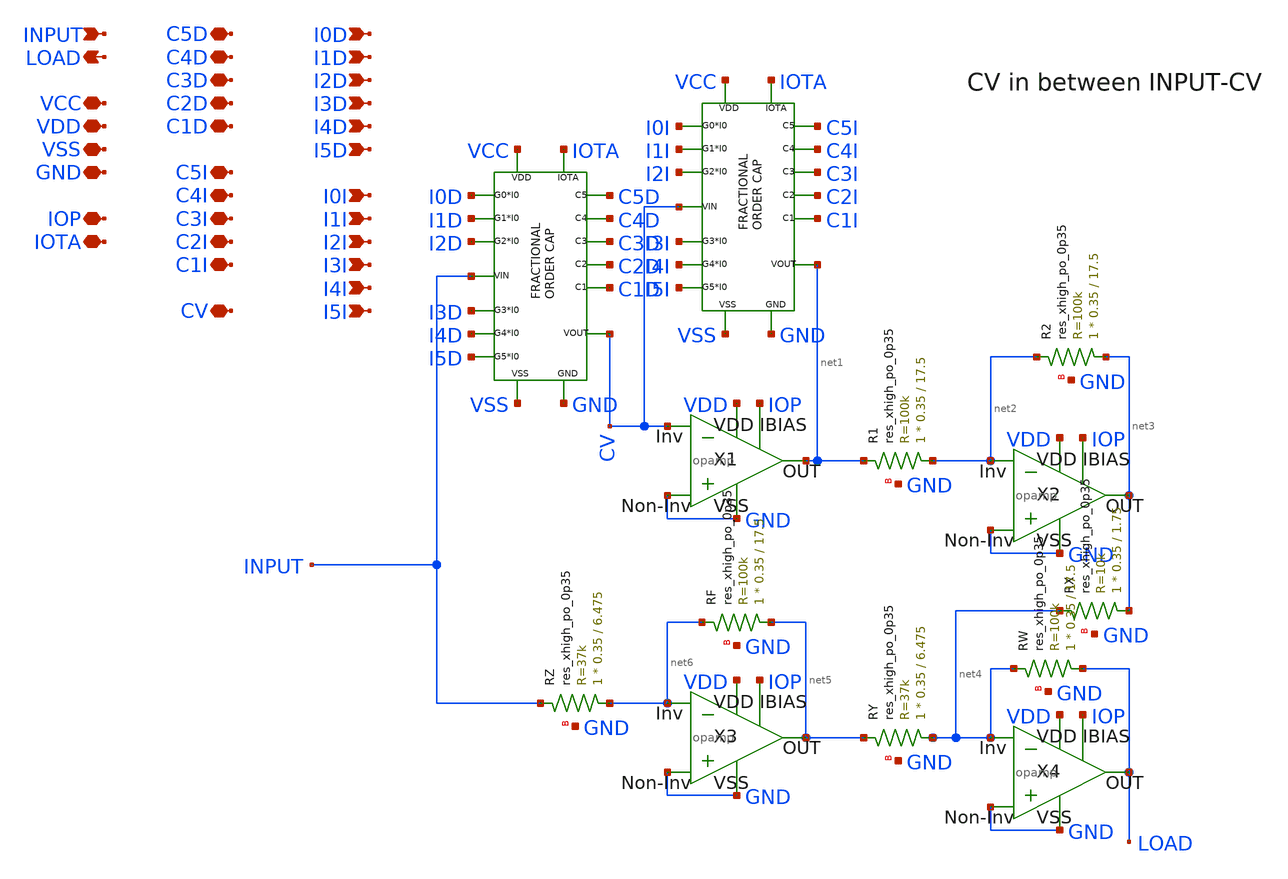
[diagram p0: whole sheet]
** sch_path: Fractional Order PID/FOPID/FOPID.sch
**.subckt FOPID VCC VDD VSS GND IOP IOTA INPUT LOAD C5D C4D C3D C2D C1D C5I C4I C3I C2I C1I I0D I1D
*+ I2D I3D I4D I5D I0I I1I I2I I3I I4I I5I CV
*.iopin VCC
*.iopin VDD
*.iopin VSS
*.iopin GND
*.iopin IOP
*.iopin IOTA
*.ipin INPUT
*.opin LOAD
*.iopin C5D
*.iopin C4D
*.iopin C3D
*.iopin C2D
*.iopin C1D
*.iopin C5I
*.iopin C4I
*.iopin C3I
*.iopin C2I
*.iopin C1I
*.ipin I0D
*.ipin I1D
*.ipin I2D
*.ipin I3D
*.ipin I4D
*.ipin I5D
*.ipin I0I
*.ipin I1I
*.ipin I2I
*.ipin I3I
*.ipin I4I
*.ipin I5I
*.iopin CV
X1 CV GND GND VDD net1 IOP opamp
X2 net2 GND GND VDD net3 IOP opamp
X3 net6 GND GND VDD net5 IOP opamp
X4 net4 GND GND VDD LOAD IOP opamp
X5 VCC IOTA CV GND VSS I5D I4D I3D I2D I1D I0D INPUT C5D C4D C3D C2D C1D Fractional_diff
X6 VCC IOTA net1 GND VSS I5I I4I I3I I2I I1I I0I CV C5I C4I C3I C2I C1I Fractional_diff
XR1 net2 net1 GND sky130_fd_pr__res_xhigh_po_0p35 L=17.5 mult=1 m=1
XR2 net3 net2 GND sky130_fd_pr__res_xhigh_po_0p35 L=17.5 mult=1 m=1
XRX net3 net4 GND sky130_fd_pr__res_xhigh_po_0p35 L=1.75 mult=1 m=1
XRW LOAD net4 GND sky130_fd_pr__res_xhigh_po_0p35 L=17.5 mult=1 m=1
XRY net4 net5 GND sky130_fd_pr__res_xhigh_po_0p35 L=6.475 mult=1 m=1
XRF net5 net6 GND sky130_fd_pr__res_xhigh_po_0p35 L=17.5 mult=1 m=1
XRZ net6 INPUT GND sky130_fd_pr__res_xhigh_po_0p35 L=6.475 mult=1 m=1
**.ends

* expanding   symbol:  /home/parallels/OPAMP/opamp.sym # of pins=6
** sym_path: /home/parallels/OPAMP/opamp.sym
** sch_path: /home/parallels/OPAMP/opamp.sch
.subckt opamp VN VP GND VDD VOUT IBIAS
*.iopin VDD
*.iopin IBIAS
*.ipin VN
*.ipin VP
*.iopin GND
*.opin VOUT
XM1 IBIAS IBIAS VDD VDD sky130_fd_pr__pfet_01v8 L=0.3 W=3 nf=1 ad='int((nf+1)/2) * W/nf * 0.29' as='int((nf+2)/2) * W/nf * 0.29'
+ pd='2*int((nf+1)/2) * (W/nf + 0.29)' ps='2*int((nf+2)/2) * (W/nf + 0.29)' nrd='0.29 / W' nrs='0.29 / W'
+ sa=0 sb=0 sd=0 mult=1 m=1
XM2 net1 IBIAS VDD VDD sky130_fd_pr__pfet_01v8 L=0.3 W=30 nf=5 ad='int((nf+1)/2) * W/nf * 0.29' as='int((nf+2)/2) * W/nf * 0.29'
+ pd='2*int((nf+1)/2) * (W/nf + 0.29)' ps='2*int((nf+2)/2) * (W/nf + 0.29)' nrd='0.29 / W' nrs='0.29 / W'
+ sa=0 sb=0 sd=0 mult=1 m=1
XM3 net2 VN net1 VDD sky130_fd_pr__pfet_01v8 L=0.3 W=36 nf=6 ad='int((nf+1)/2) * W/nf * 0.29' as='int((nf+2)/2) * W/nf * 0.29'
+ pd='2*int((nf+1)/2) * (W/nf + 0.29)' ps='2*int((nf+2)/2) * (W/nf + 0.29)' nrd='0.29 / W' nrs='0.29 / W'
+ sa=0 sb=0 sd=0 mult=1 m=1
XM4 o1 VP net1 VDD sky130_fd_pr__pfet_01v8 L=0.3 W=36 nf=6 ad='int((nf+1)/2) * W/nf * 0.29' as='int((nf+2)/2) * W/nf * 0.29'
+ pd='2*int((nf+1)/2) * (W/nf + 0.29)' ps='2*int((nf+2)/2) * (W/nf + 0.29)' nrd='0.29 / W' nrs='0.29 / W'
+ sa=0 sb=0 sd=0 mult=1 m=1
XM5 net2 net2 GND GND sky130_fd_pr__nfet_01v8 L=0.3 W=6 nf=2 ad='int((nf+1)/2) * W/nf * 0.29' as='int((nf+2)/2) * W/nf * 0.29'
+ pd='2*int((nf+1)/2) * (W/nf + 0.29)' ps='2*int((nf+2)/2) * (W/nf + 0.29)' nrd='0.29 / W' nrs='0.29 / W'
+ sa=0 sb=0 sd=0 mult=1 m=1
XM6 o1 net2 GND GND sky130_fd_pr__nfet_01v8 L=0.3 W=6 nf=2 ad='int((nf+1)/2) * W/nf * 0.29' as='int((nf+2)/2) * W/nf * 0.29'
+ pd='2*int((nf+1)/2) * (W/nf + 0.29)' ps='2*int((nf+2)/2) * (W/nf + 0.29)' nrd='0.29 / W' nrs='0.29 / W'
+ sa=0 sb=0 sd=0 mult=1 m=1
XM7 VOUT IBIAS VDD VDD sky130_fd_pr__pfet_01v8 L=0.3 W=45 nf=9 ad='int((nf+1)/2) * W/nf * 0.29' as='int((nf+2)/2) * W/nf * 0.29'
+ pd='2*int((nf+1)/2) * (W/nf + 0.29)' ps='2*int((nf+2)/2) * (W/nf + 0.29)' nrd='0.29 / W' nrs='0.29 / W'
+ sa=0 sb=0 sd=0 mult=1 m=1
XM8 VOUT o1 GND GND sky130_fd_pr__nfet_01v8 L=0.3 W=18 nf=3 ad='int((nf+1)/2) * W/nf * 0.29' as='int((nf+2)/2) * W/nf * 0.29'
+ pd='2*int((nf+1)/2) * (W/nf + 0.29)' ps='2*int((nf+2)/2) * (W/nf + 0.29)' nrd='0.29 / W' nrs='0.29 / W'
+ sa=0 sb=0 sd=0 mult=1 m=1
XC2 o1 VOUT sky130_fd_pr__cap_mim_m3_1 W=11 L=22 MF=1 m=1
.ends


* expanding   symbol:  /home/parallels/Fractional Differentiator/Fractional_diff.sym # of pins=17
** sym_path: Fractional Order PID/Fractional Order Capacitor/Fractional_diff.sym
** sch_path: Fractional Order PID/Fractional Order Capacitor/Fractional_diff.sch
.subckt Fractional_diff VDD IOTA VOUT GND VSS I5 I4 I3 I2 I1 I0 VIN C5 C4 C3 C2 C1
*.ipin VIN
*.ipin I0
*.ipin I1
*.ipin I2
*.ipin I3
*.ipin I4
*.ipin I5
*.iopin IOTA
*.iopin VDD
*.iopin VSS
*.iopin GND
*.opin VOUT
*.iopin C5
*.iopin C4
*.iopin C3
*.iopin C2
*.iopin C1
X1 IOTA VDD C5 VSS VOUT GND ota3
X2 IOTA VDD C4 VSS VOUT C5 ota3
X3 IOTA VDD C3 VSS VOUT C4 ota3
X4 IOTA VDD C2 VSS VOUT C3 ota3
X5 IOTA VDD C1 VSS VOUT C2 ota3
X6 IOTA VDD VOUT VSS GND C1 ota3
X7 IOTA VDD VOUT VSS VOUT GND ota3
X8 I5 VDD VOUT VSS GND VIN ota3
X9 I4 VDD C1 VSS GND VIN ota3
X10 I3 VDD C2 VSS GND VIN ota3
X11 I2 VDD C3 VSS GND VIN ota3
X12 I1 VDD C4 VSS GND VIN ota3
X13 I0 VDD C5 VSS GND VIN ota3
.ends


* expanding   symbol:  /home/parallels/OTA/ota3.sym # of pins=6
** sym_path: Fractional Order PID/OTA/ota3.sym
** sch_path: Fractional Order PID/OTA/ota3.sch
.subckt ota3 IBIAS VDD IOUT VSS VN VP
*.iopin VP
*.iopin IBIAS
*.iopin IOUT
*.iopin VDD
*.iopin VSS
*.iopin VN
XMp1 net1 net1 VDD VDD sky130_fd_pr__pfet_01v8 L=2 W=10 nf=2 ad='int((nf+1)/2) * W/nf * 0.29' as='int((nf+2)/2) * W/nf * 0.29'
+ pd='2*int((nf+1)/2) * (W/nf + 0.29)' ps='2*int((nf+2)/2) * (W/nf + 0.29)' nrd='0.29 / W' nrs='0.29 / W'
+ sa=0 sb=0 sd=0 mult=1 m=1
XMp2 IOUT net1 VDD VDD sky130_fd_pr__pfet_01v8 L=2 W=10 nf=2 ad='int((nf+1)/2) * W/nf * 0.29' as='int((nf+2)/2) * W/nf * 0.29'
+ pd='2*int((nf+1)/2) * (W/nf + 0.29)' ps='2*int((nf+2)/2) * (W/nf + 0.29)' nrd='0.29 / W' nrs='0.29 / W'
+ sa=0 sb=0 sd=0 mult=1 m=1
XMn1 net1 VP net2 net2 sky130_fd_pr__nfet_01v8 L=5 W=25 nf=5 ad='int((nf+1)/2) * W/nf * 0.29' as='int((nf+2)/2) * W/nf * 0.29'
+ pd='2*int((nf+1)/2) * (W/nf + 0.29)' ps='2*int((nf+2)/2) * (W/nf + 0.29)' nrd='0.29 / W' nrs='0.29 / W'
+ sa=0 sb=0 sd=0 mult=1 m=1
XMn2 IOUT VN net2 net2 sky130_fd_pr__nfet_01v8 L=5 W=5 nf=1 ad='int((nf+1)/2) * W/nf * 0.29' as='int((nf+2)/2) * W/nf * 0.29'
+ pd='2*int((nf+1)/2) * (W/nf + 0.29)' ps='2*int((nf+2)/2) * (W/nf + 0.29)' nrd='0.29 / W' nrs='0.29 / W'
+ sa=0 sb=0 sd=0 mult=1 m=1
XMn3 net1 VP net3 net3 sky130_fd_pr__nfet_01v8 L=5 W=5 nf=1 ad='int((nf+1)/2) * W/nf * 0.29' as='int((nf+2)/2) * W/nf * 0.29'
+ pd='2*int((nf+1)/2) * (W/nf + 0.29)' ps='2*int((nf+2)/2) * (W/nf + 0.29)' nrd='0.29 / W' nrs='0.29 / W'
+ sa=0 sb=0 sd=0 mult=1 m=1
XMn4 IOUT VN net3 net3 sky130_fd_pr__nfet_01v8 L=5 W=25 nf=5 ad='int((nf+1)/2) * W/nf * 0.29' as='int((nf+2)/2) * W/nf * 0.29'
+ pd='2*int((nf+1)/2) * (W/nf + 0.29)' ps='2*int((nf+2)/2) * (W/nf + 0.29)' nrd='0.29 / W' nrs='0.29 / W'
+ sa=0 sb=0 sd=0 mult=1 m=1
XMb2 net2 IBIAS VSS VSS sky130_fd_pr__nfet_01v8 L=1.5 W=60 nf=12 ad='int((nf+1)/2) * W/nf * 0.29' as='int((nf+2)/2) * W/nf * 0.29'
+ pd='2*int((nf+1)/2) * (W/nf + 0.29)' ps='2*int((nf+2)/2) * (W/nf + 0.29)' nrd='0.29 / W' nrs='0.29 / W'
+ sa=0 sb=0 sd=0 mult=1 m=1
XMb1 IBIAS IBIAS VSS VSS sky130_fd_pr__nfet_01v8 L=1.5 W=60 nf=12 ad='int((nf+1)/2) * W/nf * 0.29' as='int((nf+2)/2) * W/nf * 0.29'
+ pd='2*int((nf+1)/2) * (W/nf + 0.29)' ps='2*int((nf+2)/2) * (W/nf + 0.29)' nrd='0.29 / W' nrs='0.29 / W'
+ sa=0 sb=0 sd=0 mult=1 m=1
XMb3 net3 IBIAS VSS VSS sky130_fd_pr__nfet_01v8 L=1.5 W=60 nf=12 ad='int((nf+1)/2) * W/nf * 0.29' as='int((nf+2)/2) * W/nf * 0.29'
+ pd='2*int((nf+1)/2) * (W/nf + 0.29)' ps='2*int((nf+2)/2) * (W/nf + 0.29)' nrd='0.29 / W' nrs='0.29 / W'
+ sa=0 sb=0 sd=0 mult=1 m=1
.ends

.end
